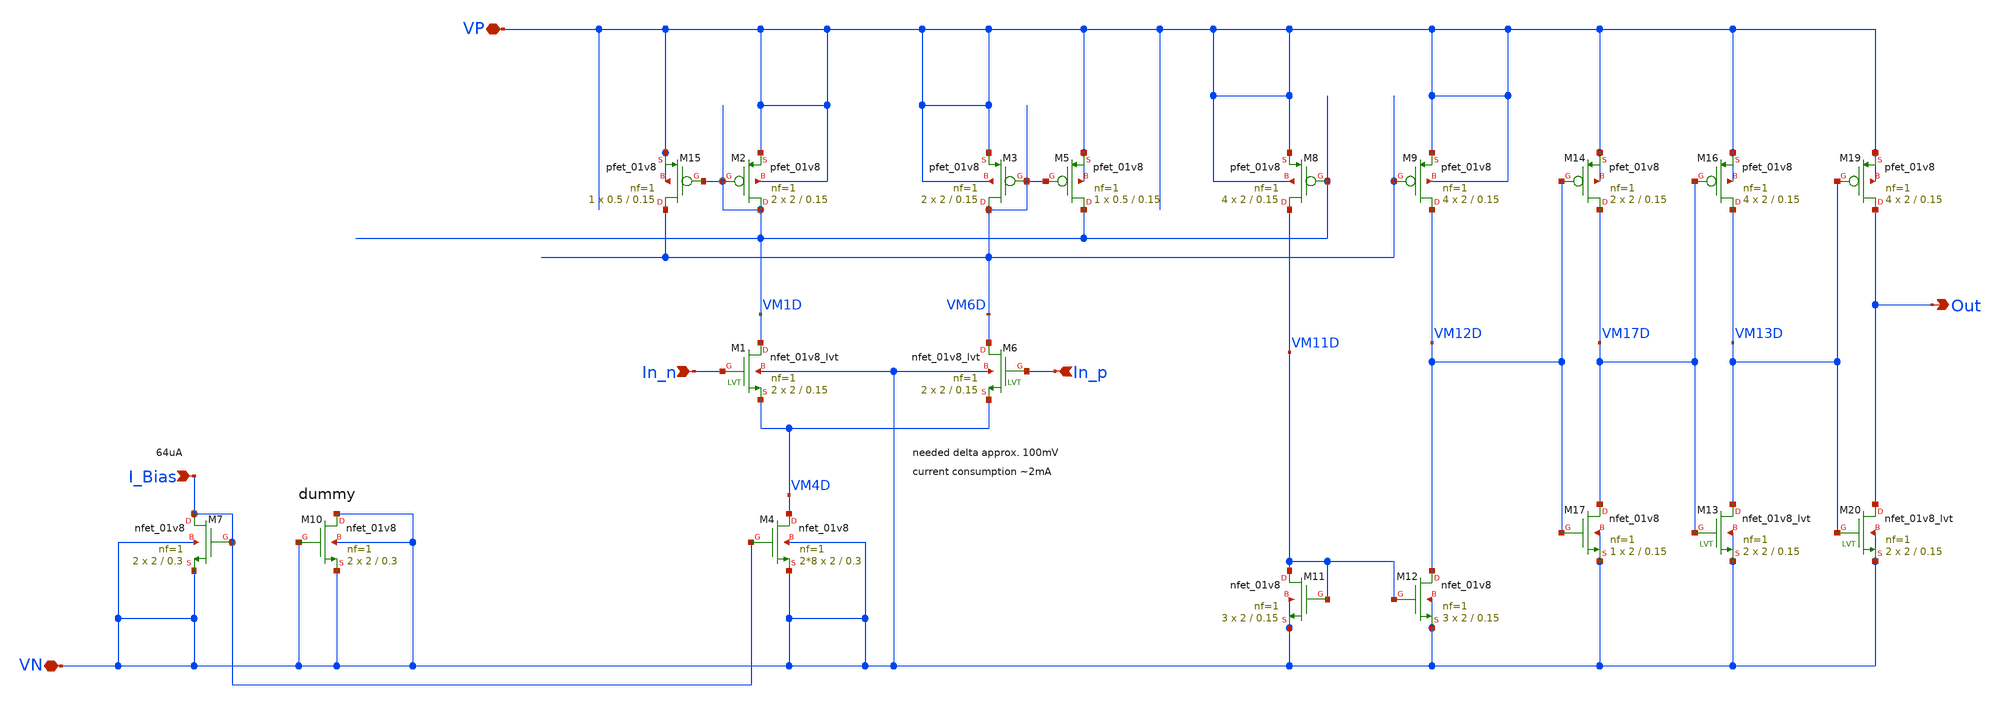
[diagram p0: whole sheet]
** sch_path: xschem/comp/comp_to_logic.sch
**.subckt comp_to_logic VP VN In_p In_n I_Bias Out
*.iopin VP
*.iopin VN
*.ipin In_p
*.ipin In_n
*.ipin I_Bias
*.opin Out
XM1 VM1D In_n VM4D VN sky130_fd_pr__nfet_01v8_lvt L=0.15 W=2 nf=1 ad='int((nf+1)/2) * W/nf * 0.29' as='int((nf+2)/2) * W/nf * 0.29'
+ pd='2*int((nf+1)/2) * (W/nf + 0.29)' ps='2*int((nf+2)/2) * (W/nf + 0.29)' nrd='0.29 / W' nrs='0.29 / W'
+ sa=0 sb=0 sd=0 mult=2 m=2
XM2 VM1D VM1D VP VP sky130_fd_pr__pfet_01v8 L=0.15 W=2 nf=1 ad='int((nf+1)/2) * W/nf * 0.29' as='int((nf+2)/2) * W/nf * 0.29'
+ pd='2*int((nf+1)/2) * (W/nf + 0.29)' ps='2*int((nf+2)/2) * (W/nf + 0.29)' nrd='0.29 / W' nrs='0.29 / W'
+ sa=0 sb=0 sd=0 mult=2 m=2
XM4 VM4D I_Bias VN VN sky130_fd_pr__nfet_01v8 L=0.3 W=2 nf=1 ad='int((nf+1)/2) * W/nf * 0.29' as='int((nf+2)/2) * W/nf * 0.29'
+ pd='2*int((nf+1)/2) * (W/nf + 0.29)' ps='2*int((nf+2)/2) * (W/nf + 0.29)' nrd='0.29 / W' nrs='0.29 / W'
+ sa=0 sb=0 sd=0 mult=2*8 m=2*8
XM6 VM6D In_p VM4D VN sky130_fd_pr__nfet_01v8_lvt L=0.15 W=2 nf=1 ad='int((nf+1)/2) * W/nf * 0.29' as='int((nf+2)/2) * W/nf * 0.29'
+ pd='2*int((nf+1)/2) * (W/nf + 0.29)' ps='2*int((nf+2)/2) * (W/nf + 0.29)' nrd='0.29 / W' nrs='0.29 / W'
+ sa=0 sb=0 sd=0 mult=2 m=2
XM7 I_Bias I_Bias VN VN sky130_fd_pr__nfet_01v8 L=0.3 W=2 nf=1 ad='int((nf+1)/2) * W/nf * 0.29' as='int((nf+2)/2) * W/nf * 0.29'
+ pd='2*int((nf+1)/2) * (W/nf + 0.29)' ps='2*int((nf+2)/2) * (W/nf + 0.29)' nrd='0.29 / W' nrs='0.29 / W'
+ sa=0 sb=0 sd=0 mult=2 m=2
XM3 VM6D VM6D VP VP sky130_fd_pr__pfet_01v8 L=0.15 W=2 nf=1 ad='int((nf+1)/2) * W/nf * 0.29' as='int((nf+2)/2) * W/nf * 0.29'
+ pd='2*int((nf+1)/2) * (W/nf + 0.29)' ps='2*int((nf+2)/2) * (W/nf + 0.29)' nrd='0.29 / W' nrs='0.29 / W'
+ sa=0 sb=0 sd=0 mult=2 m=2
XM8 VM11D VM1D VP VP sky130_fd_pr__pfet_01v8 L=0.15 W=2 nf=1 ad='int((nf+1)/2) * W/nf * 0.29' as='int((nf+2)/2) * W/nf * 0.29'
+ pd='2*int((nf+1)/2) * (W/nf + 0.29)' ps='2*int((nf+2)/2) * (W/nf + 0.29)' nrd='0.29 / W' nrs='0.29 / W'
+ sa=0 sb=0 sd=0 mult=4 m=4
XM9 VM12D VM6D VP VP sky130_fd_pr__pfet_01v8 L=0.15 W=2 nf=1 ad='int((nf+1)/2) * W/nf * 0.29' as='int((nf+2)/2) * W/nf * 0.29'
+ pd='2*int((nf+1)/2) * (W/nf + 0.29)' ps='2*int((nf+2)/2) * (W/nf + 0.29)' nrd='0.29 / W' nrs='0.29 / W'
+ sa=0 sb=0 sd=0 mult=4 m=4
XM11 VM11D VM11D VN VN sky130_fd_pr__nfet_01v8 L=0.15 W=2 nf=1 ad='int((nf+1)/2) * W/nf * 0.29' as='int((nf+2)/2) * W/nf * 0.29'
+ pd='2*int((nf+1)/2) * (W/nf + 0.29)' ps='2*int((nf+2)/2) * (W/nf + 0.29)' nrd='0.29 / W' nrs='0.29 / W'
+ sa=0 sb=0 sd=0 mult=3 m=3
XM12 VM12D VM11D VN VN sky130_fd_pr__nfet_01v8 L=0.15 W=2 nf=1 ad='int((nf+1)/2) * W/nf * 0.29' as='int((nf+2)/2) * W/nf * 0.29'
+ pd='2*int((nf+1)/2) * (W/nf + 0.29)' ps='2*int((nf+2)/2) * (W/nf + 0.29)' nrd='0.29 / W' nrs='0.29 / W'
+ sa=0 sb=0 sd=0 mult=3 m=3
XM14 VM17D VM12D VP VP sky130_fd_pr__pfet_01v8 L=0.15 W=2 nf=1 ad='int((nf+1)/2) * W/nf * 0.29' as='int((nf+2)/2) * W/nf * 0.29'
+ pd='2*int((nf+1)/2) * (W/nf + 0.29)' ps='2*int((nf+2)/2) * (W/nf + 0.29)' nrd='0.29 / W' nrs='0.29 / W'
+ sa=0 sb=0 sd=0 mult=2 m=2
XM16 VM13D VM17D VP VP sky130_fd_pr__pfet_01v8 L=0.15 W=2 nf=1 ad='int((nf+1)/2) * W/nf * 0.29' as='int((nf+2)/2) * W/nf * 0.29'
+ pd='2*int((nf+1)/2) * (W/nf + 0.29)' ps='2*int((nf+2)/2) * (W/nf + 0.29)' nrd='0.29 / W' nrs='0.29 / W'
+ sa=0 sb=0 sd=0 mult=4 m=4
XM13 VM13D VM17D VN VN sky130_fd_pr__nfet_01v8_lvt L=0.15 W=2 nf=1 ad='int((nf+1)/2) * W/nf * 0.29' as='int((nf+2)/2) * W/nf * 0.29'
+ pd='2*int((nf+1)/2) * (W/nf + 0.29)' ps='2*int((nf+2)/2) * (W/nf + 0.29)' nrd='0.29 / W' nrs='0.29 / W'
+ sa=0 sb=0 sd=0 mult=2 m=2
XM17 VM17D VM12D VN VN sky130_fd_pr__nfet_01v8 L=0.15 W=2 nf=1 ad='int((nf+1)/2) * W/nf * 0.29' as='int((nf+2)/2) * W/nf * 0.29'
+ pd='2*int((nf+1)/2) * (W/nf + 0.29)' ps='2*int((nf+2)/2) * (W/nf + 0.29)' nrd='0.29 / W' nrs='0.29 / W'
+ sa=0 sb=0 sd=0 mult=1 m=1
XM15 VM6D VM1D VP VP sky130_fd_pr__pfet_01v8 L=0.15 W=0.5 nf=1 ad='int((nf+1)/2) * W/nf * 0.29' as='int((nf+2)/2) * W/nf * 0.29'
+ pd='2*int((nf+1)/2) * (W/nf + 0.29)' ps='2*int((nf+2)/2) * (W/nf + 0.29)' nrd='0.29 / W' nrs='0.29 / W'
+ sa=0 sb=0 sd=0 mult=1 m=1
XM19 Out VM13D VP VP sky130_fd_pr__pfet_01v8 L=0.15 W=2 nf=1 ad='int((nf+1)/2) * W/nf * 0.29' as='int((nf+2)/2) * W/nf * 0.29'
+ pd='2*int((nf+1)/2) * (W/nf + 0.29)' ps='2*int((nf+2)/2) * (W/nf + 0.29)' nrd='0.29 / W' nrs='0.29 / W'
+ sa=0 sb=0 sd=0 mult=4 m=4
XM20 Out VM13D VN VN sky130_fd_pr__nfet_01v8_lvt L=0.15 W=2 nf=1 ad='int((nf+1)/2) * W/nf * 0.29' as='int((nf+2)/2) * W/nf * 0.29'
+ pd='2*int((nf+1)/2) * (W/nf + 0.29)' ps='2*int((nf+2)/2) * (W/nf + 0.29)' nrd='0.29 / W' nrs='0.29 / W'
+ sa=0 sb=0 sd=0 mult=2 m=2
XM5 VM1D VM6D VP VP sky130_fd_pr__pfet_01v8 L=0.15 W=0.5 nf=1 ad='int((nf+1)/2) * W/nf * 0.29' as='int((nf+2)/2) * W/nf * 0.29'
+ pd='2*int((nf+1)/2) * (W/nf + 0.29)' ps='2*int((nf+2)/2) * (W/nf + 0.29)' nrd='0.29 / W' nrs='0.29 / W'
+ sa=0 sb=0 sd=0 mult=1 m=1
XM10 VN VN VN VN sky130_fd_pr__nfet_01v8 L=0.3 W=2 nf=1 ad='int((nf+1)/2) * W/nf * 0.29' as='int((nf+2)/2) * W/nf * 0.29'
+ pd='2*int((nf+1)/2) * (W/nf + 0.29)' ps='2*int((nf+2)/2) * (W/nf + 0.29)' nrd='0.29 / W' nrs='0.29 / W'
+ sa=0 sb=0 sd=0 mult=2 m=2
**.ends
.end
